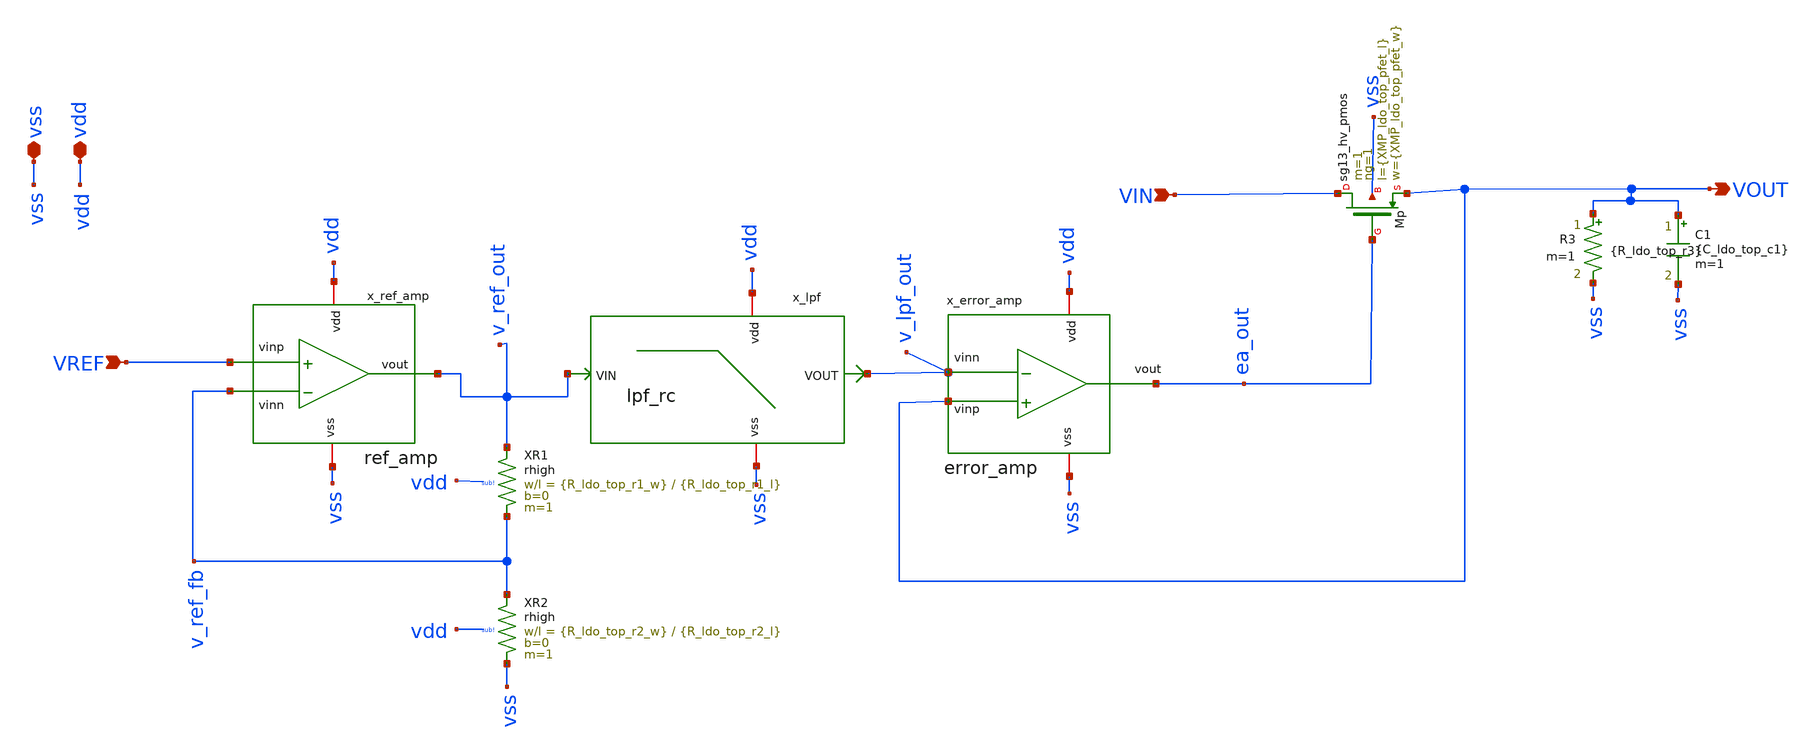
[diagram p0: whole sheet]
** sch_path: analog-db/drawings/ldo-005-ti-ldo-buffer-ref/ihp130/ldo/ldo.sch
**.subckt ldo VREF vdd vss VIN VOUT
*.ipin VREF
*.iopin vdd
*.iopin vss
*.ipin VIN
*.opin VOUT
x_ref_amp vdd v_ref_out VREF v_ref_fb vss ref_amp
XR1 v_ref_fb v_ref_out sub! rhigh w={R_ldo_top_r1_w} l={R_ldo_top_r1_l} m=1 b=0
XR2 vss v_ref_fb sub! rhigh w={R_ldo_top_r2_w} l={R_ldo_top_r2_l} m=1 b=0
x_error_amp vdd ea_out VOUT v_lpf_out vss error_amp
x_lpf net1 vss v_lpf_out v_ref_out lpf_rc
R3 VOUT vss {R_ldo_top_r3} m=1
C1 VOUT vss {C_ldo_top_c1} m=1
XMp VIN ea_out VOUT vss sg13_hv_pmos w={XMP_ldo_top_pfet_w} l={XMP_ldo_top_pfet_l} ng=1 m=1 mm_ok=1
**.ends
.end
